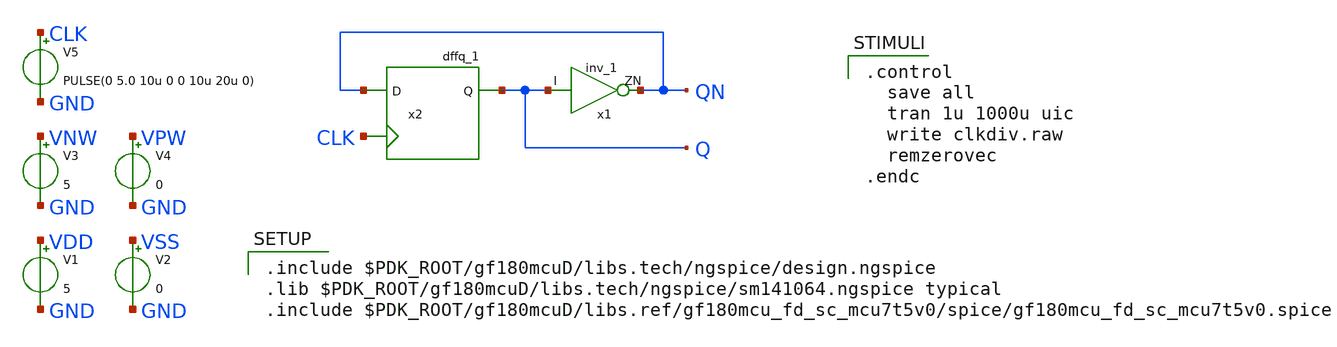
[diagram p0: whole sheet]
** sch_path: clkdiv.sch
**.subckt clkdiv
V1 VDD GND 5
V2 VSS GND 0
V3 VNW GND 5
V4 VPW GND 0
V5 CLK GND PULSE(0 5.0 10u 0 0 10u 20u 0)
x1 Q QN VDD VNW VPW VSS gf180mcu_fd_sc_mcu7t5v0__inv_1
x2 QN CLK Q VDD VNW VPW VSS gf180mcu_fd_sc_mcu7t5v0__dffq_1
**** begin user architecture code

.include $PDK_ROOT/gf180mcuD/libs.tech/ngspice/design.ngspice
.lib $PDK_ROOT/gf180mcuD/libs.tech/ngspice/sm141064.ngspice typical
.include $PDK_ROOT/gf180mcuD/libs.ref/gf180mcu_fd_sc_mcu7t5v0/spice/gf180mcu_fd_sc_mcu7t5v0.spice


.control
  save all
  tran 1u 1000u uic
  write clkdiv.raw
  remzerovec
.endc

**** end user architecture code
**.ends
.end
